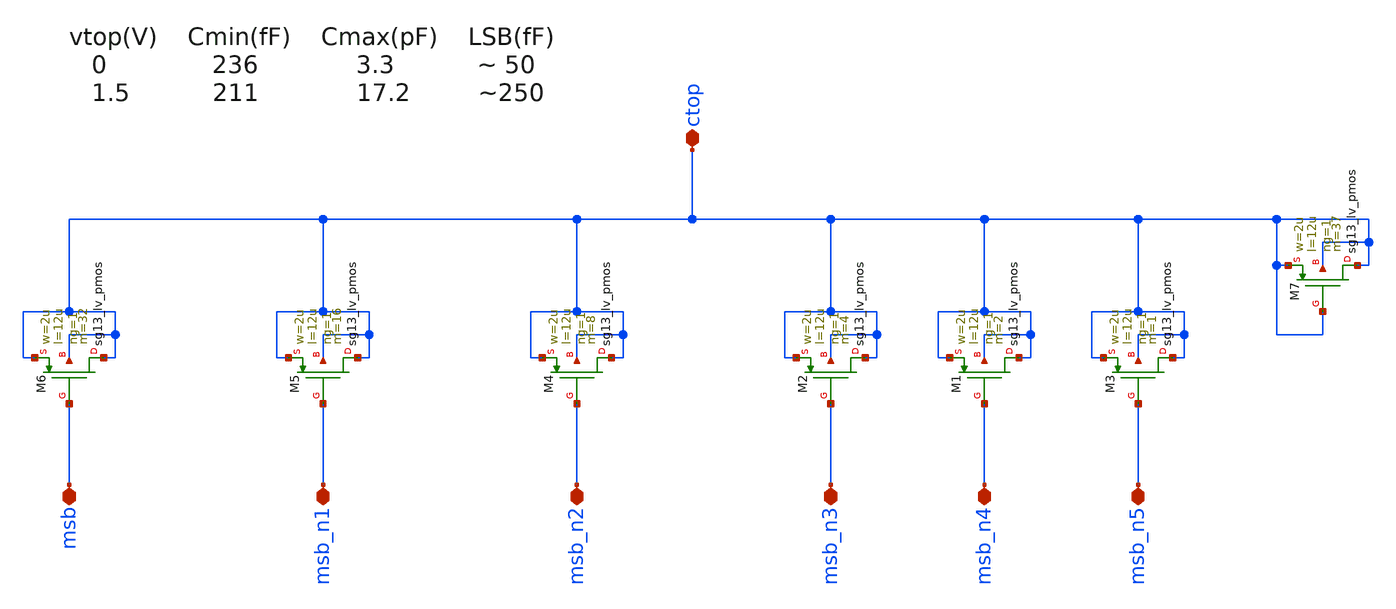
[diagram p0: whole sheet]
** sch_path: Schematics_Layout/sunrise_ro_cdac_cap_array/sunrise_ro_cdac_cap_array.sch
**.subckt sunrise_ro_cdac_cap_array msb msb_n1 msb_n2 msb_n3 msb_n4 msb_n5 ctop
*.iopin msb
*.iopin msb_n1
*.iopin msb_n2
*.iopin msb_n3
*.iopin msb_n4
*.iopin msb_n5
*.iopin ctop
XM3 ctop msb_n5 ctop ctop sg13_lv_pmos w=2u l=12u ng=1 m=1 mm_ok=1
XM1 ctop msb_n4 ctop ctop sg13_lv_pmos w=2u l=12u ng=1 m=2 mm_ok=1
XM2 ctop msb_n3 ctop ctop sg13_lv_pmos w=2u l=12u ng=1 m=4 mm_ok=1
XM4 ctop msb_n2 ctop ctop sg13_lv_pmos w=2u l=12u ng=1 m=8 mm_ok=1
XM5 ctop msb_n1 ctop ctop sg13_lv_pmos w=2u l=12u ng=1 m=16 mm_ok=1
XM6 ctop msb ctop ctop sg13_lv_pmos w=2u l=12u ng=1 m=32 mm_ok=1
XM7 ctop ctop ctop ctop sg13_lv_pmos w=2u l=12u ng=1 m=37 mm_ok=1
**.ends
.end
